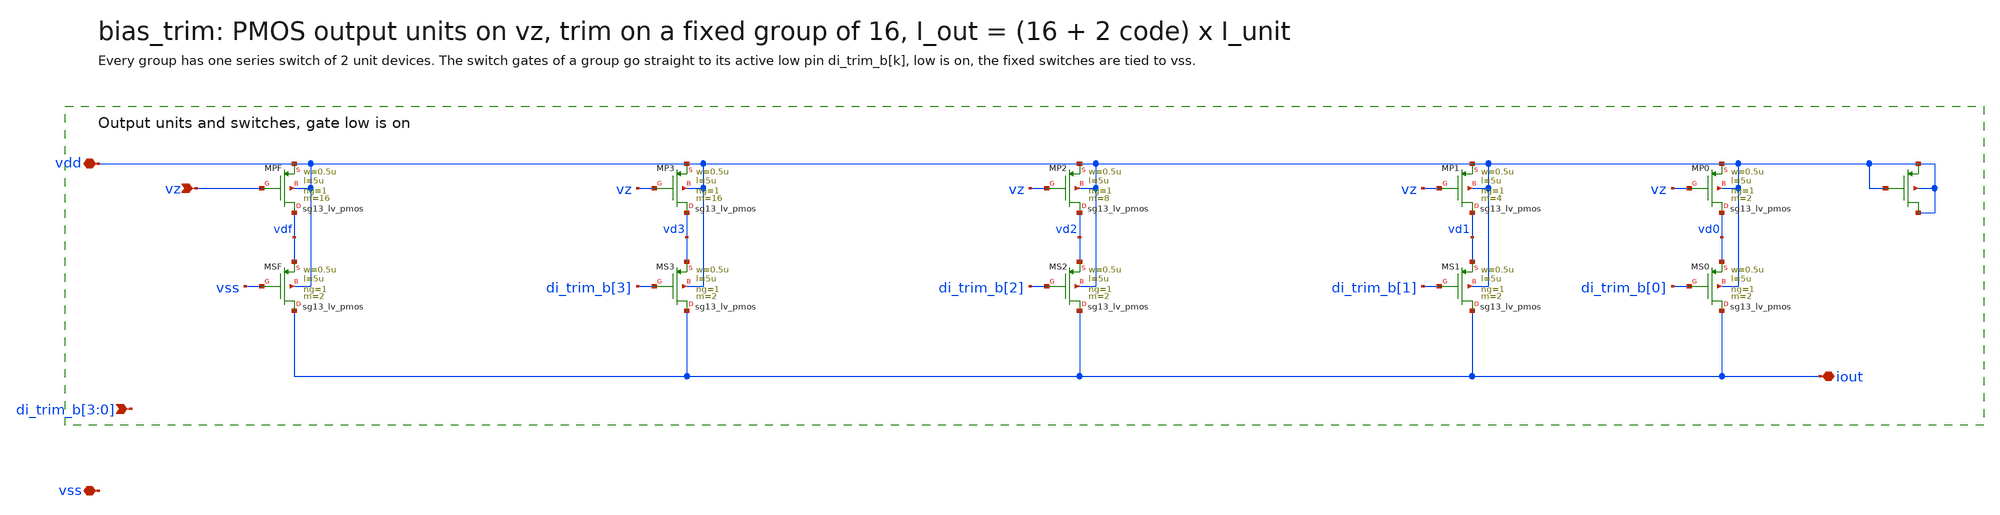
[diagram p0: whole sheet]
** sch_path: ip/dsm2_core/schematic/bias_trim.sch
**.subckt bias_trim vdd vz iout vss di_trim_b[3],di_trim_b[2],di_trim_b[1],di_trim_b[0]
*.iopin vdd
*.ipin vz
*.iopin iout
*.iopin vss
*.ipin di_trim_b[3],di_trim_b[2],di_trim_b[1],di_trim_b[0]
XMPF vdf vz vdd vdd sg13_lv_pmos w=0.5u l=5u ng=1 m=16 mm_ok=1
XMSF iout vss vdf vdd sg13_lv_pmos w=0.5u l=5u ng=1 m=2 mm_ok=1
XMP3 vd3 vz vdd vdd sg13_lv_pmos w=0.5u l=5u ng=1 m=16 mm_ok=1
XMS3 iout di_trim_b[3] vd3 vdd sg13_lv_pmos w=0.5u l=5u ng=1 m=2 mm_ok=1
XMP2 vd2 vz vdd vdd sg13_lv_pmos w=0.5u l=5u ng=1 m=8 mm_ok=1
XMS2 iout di_trim_b[2] vd2 vdd sg13_lv_pmos w=0.5u l=5u ng=1 m=2 mm_ok=1
XMP1 vd1 vz vdd vdd sg13_lv_pmos w=0.5u l=5u ng=1 m=4 mm_ok=1
XMS1 iout di_trim_b[1] vd1 vdd sg13_lv_pmos w=0.5u l=5u ng=1 m=2 mm_ok=1
XMP0 vd0 vz vdd vdd sg13_lv_pmos w=0.5u l=5u ng=1 m=2 mm_ok=1
XMS0 iout di_trim_b[0] vd0 vdd sg13_lv_pmos w=0.5u l=5u ng=1 m=2 mm_ok=1
XMPD vdd vdd vdd vdd sg13_lv_pmos w=0.5u l=5u ng=1 m=40 mm_ok=1
**.ends
.end
